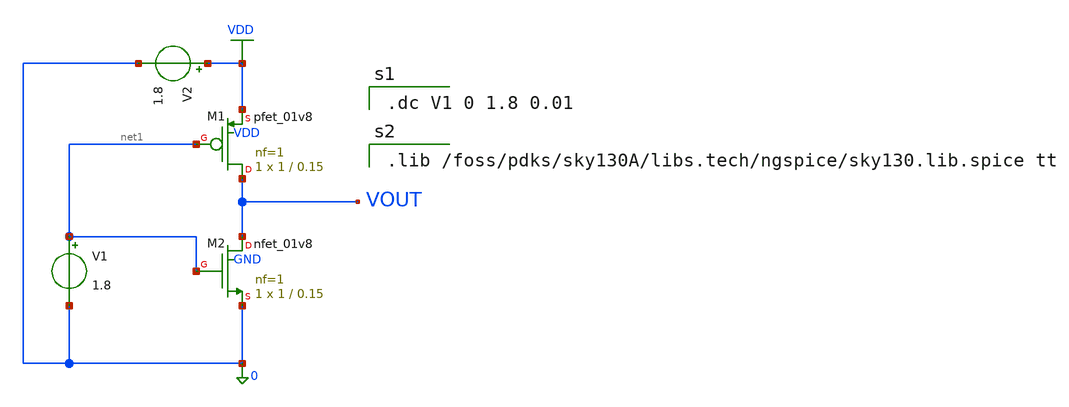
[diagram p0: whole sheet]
** sch_path: stage0/inverter/inverter.sch
**.subckt inverter
V1 net1 0 1.8
V2 VDD 0 1.8
XM1 VOUT net1 VDD VDD sky130_fd_pr__pfet_01v8 L=0.15 W=1 nf=1 ad='int((1 + 1)/2) * 1 / 1 * 0.29' as='int((1 + 2)/2) * 1 / 1 * 0.29'
+ pd='2*int((1 + 1)/2) * (1 / 1 + 0.29)' ps='2*int((1 + 2)/2) * (1 / 1 + 0.29)' nrd='0.29 / 1 ' nrs='0.29 / 1 '
+ sa=0 sb=0 sd=0 mult=1 m=1
XM2 VOUT net1 0 GND sky130_fd_pr__nfet_01v8 L=0.15 W=1 nf=1 ad='int((1 + 1)/2) * 1 / 1 * 0.29' as='int((1 + 2)/2) * 1 / 1 * 0.29'
+ pd='2*int((1 + 1)/2) * (1 / 1 + 0.29)' ps='2*int((1 + 2)/2) * (1 / 1 + 0.29)' nrd='0.29 / 1 ' nrs='0.29 / 1 '
+ sa=0 sb=0 sd=0 mult=1 m=1
**** begin user architecture code

.dc V1 0 1.8 0.01


.lib /foss/pdks/sky130A/libs.tech/ngspice/sky130.lib.spice tt

**** end user architecture code
**.ends
.GLOBAL VDD
.end
